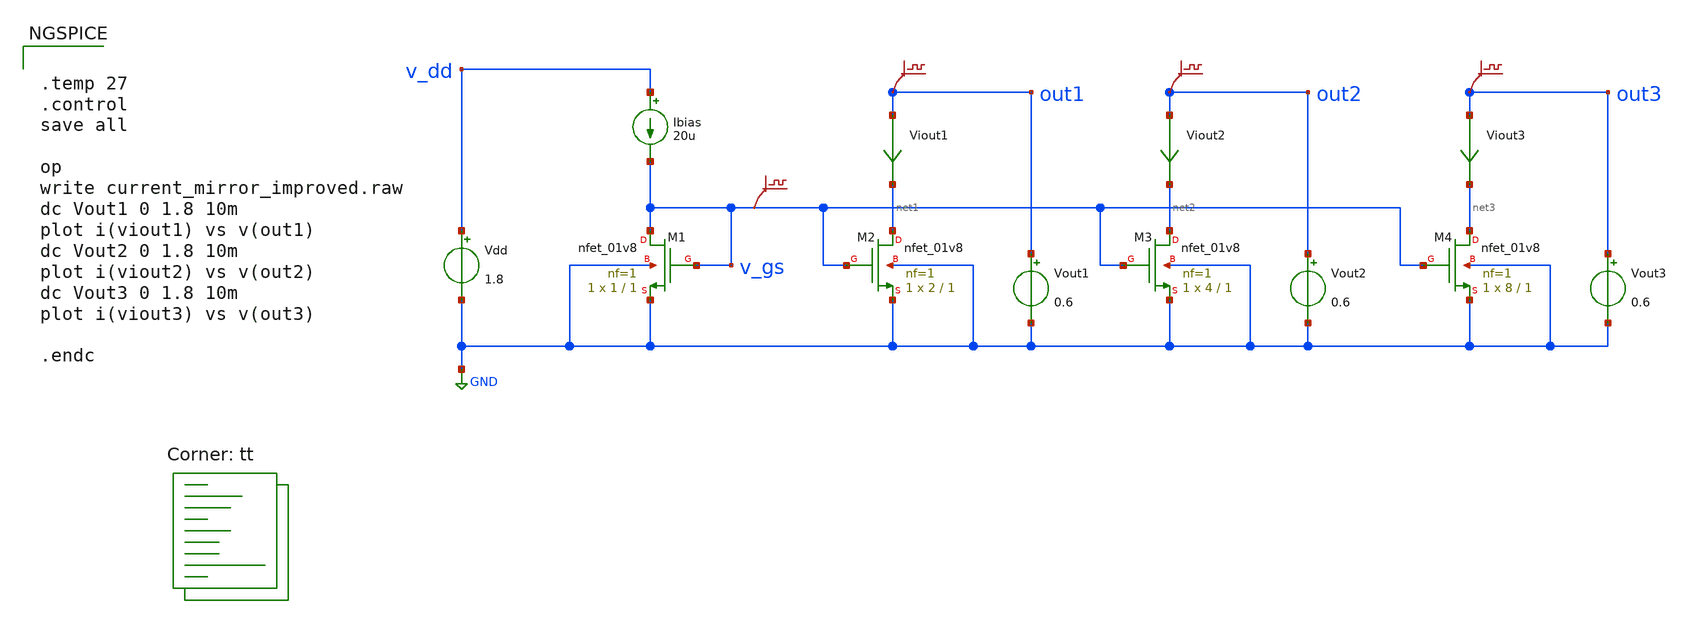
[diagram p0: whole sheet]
** sch_path: Modulo_Analogico/Lab4/current_mirror_improved.sch
**.subckt current_mirror_improved
Vdd v_dd GND 1.8
Ibias v_dd v_gs 20u
Vout1 out1 GND 0.6
Vout2 out2 GND 0.6
Vout3 out3 GND 0.6
.save v(out1)
.save v(out2)
.save v(out3)
.save v(v_gs)
Viout1 out1 net1 0
.save i(viout1)
Viout2 out2 net2 0
.save i(viout2)
Viout3 out3 net3 0
.save i(viout3)
XM1 v_gs v_gs GND GND sky130_fd_pr__nfet_01v8 L=1 W=1 nf=1 ad='int((1 + 1)/2) * 1 / 1 * 0.29' as='int((1 + 2)/2) * 1 / 1 * 0.29'
+ pd='2*int((1 + 1)/2) * (1 / 1 + 0.29)' ps='2*int((1 + 2)/2) * (1 / 1 + 0.29)' nrd='0.29 / 1 ' nrs='0.29 / 1 '
+ sa=0 sb=0 sd=0 mult=1 m=1
XM2 net1 v_gs GND GND sky130_fd_pr__nfet_01v8 L=1 W=2 nf=1 ad='int((1 + 1)/2) * 2 / 1 * 0.29' as='int((1 + 2)/2) * 2 / 1 * 0.29'
+ pd='2*int((1 + 1)/2) * (2 / 1 + 0.29)' ps='2*int((1 + 2)/2) * (2 / 1 + 0.29)' nrd='0.29 / 2 ' nrs='0.29 / 2 '
+ sa=0 sb=0 sd=0 mult=1 m=1
XM3 net2 v_gs GND GND sky130_fd_pr__nfet_01v8 L=1 W=4 nf=1 ad='int((1 + 1)/2) * 4 / 1 * 0.29' as='int((1 + 2)/2) * 4 / 1 * 0.29'
+ pd='2*int((1 + 1)/2) * (4 / 1 + 0.29)' ps='2*int((1 + 2)/2) * (4 / 1 + 0.29)' nrd='0.29 / 4 ' nrs='0.29 / 4 '
+ sa=0 sb=0 sd=0 mult=1 m=1
XM4 net3 v_gs GND GND sky130_fd_pr__nfet_01v8 L=1 W=8 nf=1 ad='int((1 + 1)/2) * 8 / 1 * 0.29' as='int((1 + 2)/2) * 8 / 1 * 0.29'
+ pd='2*int((1 + 1)/2) * (8 / 1 + 0.29)' ps='2*int((1 + 2)/2) * (8 / 1 + 0.29)' nrd='0.29 / 8 ' nrs='0.29 / 8 '
+ sa=0 sb=0 sd=0 mult=1 m=1
**** begin user architecture code


.temp 27
.control
save all

op
write current_mirror_improved.raw
dc Vout1 0 1.8 10m
plot i(viout1) vs v(out1)
dc Vout2 0 1.8 10m
plot i(viout2) vs v(out2)
dc Vout3 0 1.8 10m
plot i(viout3) vs v(out3)

.endc


.lib $::SKYWATER_MODELS/sky130.lib.spice tt
**** end user architecture code
**.ends
.GLOBAL GND
.end
